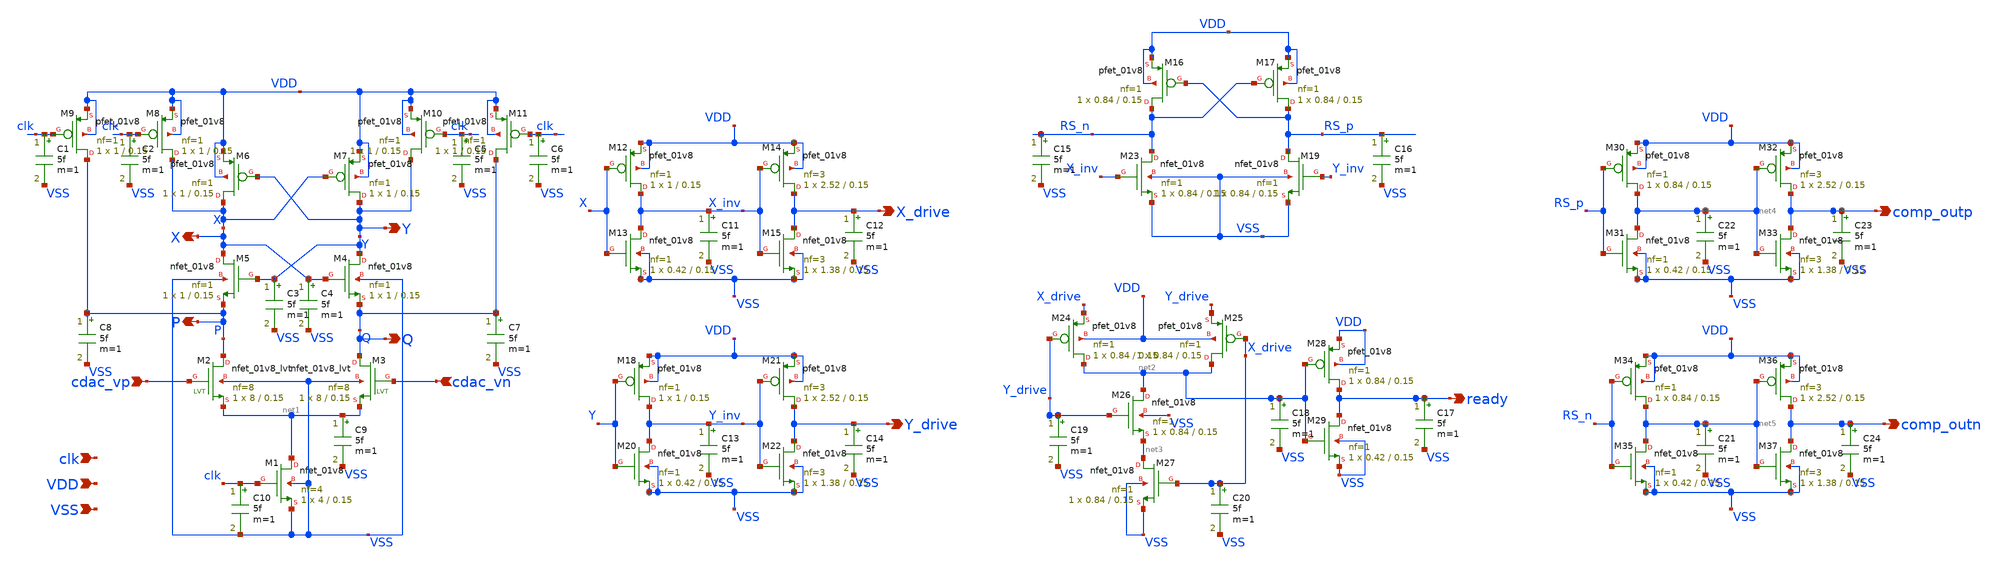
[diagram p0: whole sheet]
** sch_path: hgu/xschem/hgu_comp_withc.sch
**.subckt hgu_comp_withc cdac_vn cdac_vp VSS VDD clk X Y P Q ready X_drive Y_drive comp_outp
*+ comp_outn
*.ipin cdac_vn
*.ipin cdac_vp
*.ipin VSS
*.ipin VDD
*.ipin clk
*.opin X
*.opin Y
*.opin P
*.opin Q
*.opin ready
*.opin X_drive
*.opin Y_drive
*.opin comp_outp
*.opin comp_outn
XM1 net1 clk VSS VSS sky130_fd_pr__nfet_01v8 L=0.15 W=4 nf=4 ad='int((nf+1)/2) * W/nf * 0.29' as='int((nf+2)/2) * W/nf * 0.29'
+ pd='2*int((nf+1)/2) * (W/nf + 0.29)' ps='2*int((nf+2)/2) * (W/nf + 0.29)' nrd='0.29 / W' nrs='0.29 / W'
+ sa=0 sb=0 sd=0 mult=1 m=1
XM4 Y X Q VSS sky130_fd_pr__nfet_01v8 L=0.15 W=1 nf=1 ad='int((nf+1)/2) * W/nf * 0.29' as='int((nf+2)/2) * W/nf * 0.29'
+ pd='2*int((nf+1)/2) * (W/nf + 0.29)' ps='2*int((nf+2)/2) * (W/nf + 0.29)' nrd='0.29 / W' nrs='0.29 / W'
+ sa=0 sb=0 sd=0 mult=1 m=1
XM5 X Y P VSS sky130_fd_pr__nfet_01v8 L=0.15 W=1 nf=1 ad='int((nf+1)/2) * W/nf * 0.29' as='int((nf+2)/2) * W/nf * 0.29'
+ pd='2*int((nf+1)/2) * (W/nf + 0.29)' ps='2*int((nf+2)/2) * (W/nf + 0.29)' nrd='0.29 / W' nrs='0.29 / W'
+ sa=0 sb=0 sd=0 mult=1 m=1
XM6 X Y VDD VDD sky130_fd_pr__pfet_01v8 L=0.15 W=1 nf=1 ad='int((nf+1)/2) * W/nf * 0.29' as='int((nf+2)/2) * W/nf * 0.29'
+ pd='2*int((nf+1)/2) * (W/nf + 0.29)' ps='2*int((nf+2)/2) * (W/nf + 0.29)' nrd='0.29 / W' nrs='0.29 / W'
+ sa=0 sb=0 sd=0 mult=1 m=1
XM7 Y X VDD VDD sky130_fd_pr__pfet_01v8 L=0.15 W=1 nf=1 ad='int((nf+1)/2) * W/nf * 0.29' as='int((nf+2)/2) * W/nf * 0.29'
+ pd='2*int((nf+1)/2) * (W/nf + 0.29)' ps='2*int((nf+2)/2) * (W/nf + 0.29)' nrd='0.29 / W' nrs='0.29 / W'
+ sa=0 sb=0 sd=0 mult=1 m=1
XM8 X clk VDD VDD sky130_fd_pr__pfet_01v8 L=0.15 W=1 nf=1 ad='int((nf+1)/2) * W/nf * 0.29' as='int((nf+2)/2) * W/nf * 0.29'
+ pd='2*int((nf+1)/2) * (W/nf + 0.29)' ps='2*int((nf+2)/2) * (W/nf + 0.29)' nrd='0.29 / W' nrs='0.29 / W'
+ sa=0 sb=0 sd=0 mult=1 m=1
XM9 P clk VDD VDD sky130_fd_pr__pfet_01v8 L=0.15 W=1 nf=1 ad='int((nf+1)/2) * W/nf * 0.29' as='int((nf+2)/2) * W/nf * 0.29'
+ pd='2*int((nf+1)/2) * (W/nf + 0.29)' ps='2*int((nf+2)/2) * (W/nf + 0.29)' nrd='0.29 / W' nrs='0.29 / W'
+ sa=0 sb=0 sd=0 mult=1 m=1
XM10 Y clk VDD VDD sky130_fd_pr__pfet_01v8 L=0.15 W=1 nf=1 ad='int((nf+1)/2) * W/nf * 0.29' as='int((nf+2)/2) * W/nf * 0.29'
+ pd='2*int((nf+1)/2) * (W/nf + 0.29)' ps='2*int((nf+2)/2) * (W/nf + 0.29)' nrd='0.29 / W' nrs='0.29 / W'
+ sa=0 sb=0 sd=0 mult=1 m=1
XM11 Q clk VDD VDD sky130_fd_pr__pfet_01v8 L=0.15 W=1 nf=1 ad='int((nf+1)/2) * W/nf * 0.29' as='int((nf+2)/2) * W/nf * 0.29'
+ pd='2*int((nf+1)/2) * (W/nf + 0.29)' ps='2*int((nf+2)/2) * (W/nf + 0.29)' nrd='0.29 / W' nrs='0.29 / W'
+ sa=0 sb=0 sd=0 mult=1 m=1
XM16 RS_n RS_p VDD VDD sky130_fd_pr__pfet_01v8 L=0.15 W=0.84 nf=1 ad='int((nf+1)/2) * W/nf * 0.29' as='int((nf+2)/2) * W/nf * 0.29'
+ pd='2*int((nf+1)/2) * (W/nf + 0.29)' ps='2*int((nf+2)/2) * (W/nf + 0.29)' nrd='0.29 / W' nrs='0.29 / W'
+ sa=0 sb=0 sd=0 mult=1 m=1
XM17 RS_p RS_n VDD VDD sky130_fd_pr__pfet_01v8 L=0.15 W=0.84 nf=1 ad='int((nf+1)/2) * W/nf * 0.29' as='int((nf+2)/2) * W/nf * 0.29'
+ pd='2*int((nf+1)/2) * (W/nf + 0.29)' ps='2*int((nf+2)/2) * (W/nf + 0.29)' nrd='0.29 / W' nrs='0.29 / W'
+ sa=0 sb=0 sd=0 mult=1 m=1
XM19 RS_p Y_inv VSS VSS sky130_fd_pr__nfet_01v8 L=0.15 W=0.84 nf=1 ad='int((nf+1)/2) * W/nf * 0.29' as='int((nf+2)/2) * W/nf * 0.29'
+ pd='2*int((nf+1)/2) * (W/nf + 0.29)' ps='2*int((nf+2)/2) * (W/nf + 0.29)' nrd='0.29 / W' nrs='0.29 / W'
+ sa=0 sb=0 sd=0 mult=1 m=1
XM23 RS_n X_inv VSS VSS sky130_fd_pr__nfet_01v8 L=0.15 W=0.84 nf=1 ad='int((nf+1)/2) * W/nf * 0.29' as='int((nf+2)/2) * W/nf * 0.29'
+ pd='2*int((nf+1)/2) * (W/nf + 0.29)' ps='2*int((nf+2)/2) * (W/nf + 0.29)' nrd='0.29 / W' nrs='0.29 / W'
+ sa=0 sb=0 sd=0 mult=1 m=1
XM2 P cdac_vp net1 VSS sky130_fd_pr__nfet_01v8_lvt L=0.15 W=8 nf=8 ad='int((nf+1)/2) * W / nf * 0.29'
+ as='int((nf+2)/2) * W / nf * 0.29' pd='2*int((nf+1)/2) * (W / nf + 0.29)' ps='2*int((nf+2)/2) * (W / nf + 0.29)'
+ nrd='0.29 / W ' nrs='0.29 / W ' sa=0 sb=0 sd=0 mult=1 m=1
XM3 Q cdac_vn net1 VSS sky130_fd_pr__nfet_01v8_lvt L=0.15 W=8 nf=8 ad='int((nf+1)/2) * W / nf * 0.29'
+ as='int((nf+2)/2) * W / nf * 0.29' pd='2*int((nf+1)/2) * (W / nf + 0.29)' ps='2*int((nf+2)/2) * (W / nf + 0.29)'
+ nrd='0.29 / W ' nrs='0.29 / W ' sa=0 sb=0 sd=0 mult=1 m=1
XM12 X_inv X VDD VDD sky130_fd_pr__pfet_01v8 L=0.15 W=1 nf=1 ad='int((nf+1)/2) * W/nf * 0.29' as='int((nf+2)/2) * W/nf * 0.29'
+ pd='2*int((nf+1)/2) * (W/nf + 0.29)' ps='2*int((nf+2)/2) * (W/nf + 0.29)' nrd='0.29 / W' nrs='0.29 / W'
+ sa=0 sb=0 sd=0 mult=1 m=1
XM13 X_inv X VSS VSS sky130_fd_pr__nfet_01v8 L=0.15 W=0.42 nf=1 ad='int((nf+1)/2) * W/nf * 0.29' as='int((nf+2)/2) * W/nf * 0.29'
+ pd='2*int((nf+1)/2) * (W/nf + 0.29)' ps='2*int((nf+2)/2) * (W/nf + 0.29)' nrd='0.29 / W' nrs='0.29 / W'
+ sa=0 sb=0 sd=0 mult=1 m=1
XM14 X_drive X_inv VDD VDD sky130_fd_pr__pfet_01v8 L=0.15 W=2.52 nf=3 ad='int((nf+1)/2) * W/nf * 0.29'
+ as='int((nf+2)/2) * W/nf * 0.29' pd='2*int((nf+1)/2) * (W/nf + 0.29)' ps='2*int((nf+2)/2) * (W/nf + 0.29)'
+ nrd='0.29 / W' nrs='0.29 / W' sa=0 sb=0 sd=0 mult=1 m=1
XM15 X_drive X_inv VSS VSS sky130_fd_pr__nfet_01v8 L=0.15 W=1.38 nf=3 ad='int((nf+1)/2) * W/nf * 0.29'
+ as='int((nf+2)/2) * W/nf * 0.29' pd='2*int((nf+1)/2) * (W/nf + 0.29)' ps='2*int((nf+2)/2) * (W/nf + 0.29)'
+ nrd='0.29 / W' nrs='0.29 / W' sa=0 sb=0 sd=0 mult=1 m=1
XM18 Y_inv Y VDD VDD sky130_fd_pr__pfet_01v8 L=0.15 W=1 nf=1 ad='int((nf+1)/2) * W/nf * 0.29' as='int((nf+2)/2) * W/nf * 0.29'
+ pd='2*int((nf+1)/2) * (W/nf + 0.29)' ps='2*int((nf+2)/2) * (W/nf + 0.29)' nrd='0.29 / W' nrs='0.29 / W'
+ sa=0 sb=0 sd=0 mult=1 m=1
XM20 Y_inv Y VSS VSS sky130_fd_pr__nfet_01v8 L=0.15 W=0.42 nf=1 ad='int((nf+1)/2) * W/nf * 0.29' as='int((nf+2)/2) * W/nf * 0.29'
+ pd='2*int((nf+1)/2) * (W/nf + 0.29)' ps='2*int((nf+2)/2) * (W/nf + 0.29)' nrd='0.29 / W' nrs='0.29 / W'
+ sa=0 sb=0 sd=0 mult=1 m=1
XM21 Y_drive Y_inv VDD VDD sky130_fd_pr__pfet_01v8 L=0.15 W=2.52 nf=3 ad='int((nf+1)/2) * W/nf * 0.29'
+ as='int((nf+2)/2) * W/nf * 0.29' pd='2*int((nf+1)/2) * (W/nf + 0.29)' ps='2*int((nf+2)/2) * (W/nf + 0.29)'
+ nrd='0.29 / W' nrs='0.29 / W' sa=0 sb=0 sd=0 mult=1 m=1
XM22 Y_drive Y_inv VSS VSS sky130_fd_pr__nfet_01v8 L=0.15 W=1.38 nf=3 ad='int((nf+1)/2) * W/nf * 0.29'
+ as='int((nf+2)/2) * W/nf * 0.29' pd='2*int((nf+1)/2) * (W/nf + 0.29)' ps='2*int((nf+2)/2) * (W/nf + 0.29)'
+ nrd='0.29 / W' nrs='0.29 / W' sa=0 sb=0 sd=0 mult=1 m=1
XM24 net2 Y_drive X_drive VDD sky130_fd_pr__pfet_01v8 L=0.15 W=0.84 nf=1 ad='int((nf+1)/2) * W/nf * 0.29'
+ as='int((nf+2)/2) * W/nf * 0.29' pd='2*int((nf+1)/2) * (W/nf + 0.29)' ps='2*int((nf+2)/2) * (W/nf + 0.29)'
+ nrd='0.29 / W' nrs='0.29 / W' sa=0 sb=0 sd=0 mult=1 m=1
XM25 net2 X_drive Y_drive VDD sky130_fd_pr__pfet_01v8 L=0.15 W=0.84 nf=1 ad='int((nf+1)/2) * W/nf * 0.29'
+ as='int((nf+2)/2) * W/nf * 0.29' pd='2*int((nf+1)/2) * (W/nf + 0.29)' ps='2*int((nf+2)/2) * (W/nf + 0.29)'
+ nrd='0.29 / W' nrs='0.29 / W' sa=0 sb=0 sd=0 mult=1 m=1
XM26 net2 Y_drive net3 VSS sky130_fd_pr__nfet_01v8 L=0.15 W=0.84 nf=1 ad='int((nf+1)/2) * W/nf * 0.29'
+ as='int((nf+2)/2) * W/nf * 0.29' pd='2*int((nf+1)/2) * (W/nf + 0.29)' ps='2*int((nf+2)/2) * (W/nf + 0.29)'
+ nrd='0.29 / W' nrs='0.29 / W' sa=0 sb=0 sd=0 mult=1 m=1
XM27 net3 X_drive VSS VSS sky130_fd_pr__nfet_01v8 L=0.15 W=0.84 nf=1 ad='int((nf+1)/2) * W/nf * 0.29'
+ as='int((nf+2)/2) * W/nf * 0.29' pd='2*int((nf+1)/2) * (W/nf + 0.29)' ps='2*int((nf+2)/2) * (W/nf + 0.29)'
+ nrd='0.29 / W' nrs='0.29 / W' sa=0 sb=0 sd=0 mult=1 m=1
XM28 ready net2 VDD VDD sky130_fd_pr__pfet_01v8 L=0.15 W=0.84 nf=1 ad='int((nf+1)/2) * W/nf * 0.29' as='int((nf+2)/2) * W/nf * 0.29'
+ pd='2*int((nf+1)/2) * (W/nf + 0.29)' ps='2*int((nf+2)/2) * (W/nf + 0.29)' nrd='0.29 / W' nrs='0.29 / W'
+ sa=0 sb=0 sd=0 mult=1 m=1
XM29 ready net2 VSS VSS sky130_fd_pr__nfet_01v8 L=0.15 W=0.42 nf=1 ad='int((nf+1)/2) * W/nf * 0.29' as='int((nf+2)/2) * W/nf * 0.29'
+ pd='2*int((nf+1)/2) * (W/nf + 0.29)' ps='2*int((nf+2)/2) * (W/nf + 0.29)' nrd='0.29 / W' nrs='0.29 / W'
+ sa=0 sb=0 sd=0 mult=1 m=1
XM30 net4 RS_p VDD VDD sky130_fd_pr__pfet_01v8 L=0.15 W=0.84 nf=1 ad='int((nf+1)/2) * W/nf * 0.29' as='int((nf+2)/2) * W/nf * 0.29'
+ pd='2*int((nf+1)/2) * (W/nf + 0.29)' ps='2*int((nf+2)/2) * (W/nf + 0.29)' nrd='0.29 / W' nrs='0.29 / W'
+ sa=0 sb=0 sd=0 mult=1 m=1
XM31 net4 RS_p VSS VSS sky130_fd_pr__nfet_01v8 L=0.15 W=0.42 nf=1 ad='int((nf+1)/2) * W/nf * 0.29' as='int((nf+2)/2) * W/nf * 0.29'
+ pd='2*int((nf+1)/2) * (W/nf + 0.29)' ps='2*int((nf+2)/2) * (W/nf + 0.29)' nrd='0.29 / W' nrs='0.29 / W'
+ sa=0 sb=0 sd=0 mult=1 m=1
XM32 comp_outp net4 VDD VDD sky130_fd_pr__pfet_01v8 L=0.15 W=2.52 nf=3 ad='int((nf+1)/2) * W/nf * 0.29'
+ as='int((nf+2)/2) * W/nf * 0.29' pd='2*int((nf+1)/2) * (W/nf + 0.29)' ps='2*int((nf+2)/2) * (W/nf + 0.29)'
+ nrd='0.29 / W' nrs='0.29 / W' sa=0 sb=0 sd=0 mult=1 m=1
XM33 comp_outp net4 VSS VSS sky130_fd_pr__nfet_01v8 L=0.15 W=1.38 nf=3 ad='int((nf+1)/2) * W/nf * 0.29'
+ as='int((nf+2)/2) * W/nf * 0.29' pd='2*int((nf+1)/2) * (W/nf + 0.29)' ps='2*int((nf+2)/2) * (W/nf + 0.29)'
+ nrd='0.29 / W' nrs='0.29 / W' sa=0 sb=0 sd=0 mult=1 m=1
XM34 net5 RS_n VDD VDD sky130_fd_pr__pfet_01v8 L=0.15 W=0.84 nf=1 ad='int((nf+1)/2) * W/nf * 0.29' as='int((nf+2)/2) * W/nf * 0.29'
+ pd='2*int((nf+1)/2) * (W/nf + 0.29)' ps='2*int((nf+2)/2) * (W/nf + 0.29)' nrd='0.29 / W' nrs='0.29 / W'
+ sa=0 sb=0 sd=0 mult=1 m=1
XM35 net5 RS_n VSS VSS sky130_fd_pr__nfet_01v8 L=0.15 W=0.42 nf=1 ad='int((nf+1)/2) * W/nf * 0.29' as='int((nf+2)/2) * W/nf * 0.29'
+ pd='2*int((nf+1)/2) * (W/nf + 0.29)' ps='2*int((nf+2)/2) * (W/nf + 0.29)' nrd='0.29 / W' nrs='0.29 / W'
+ sa=0 sb=0 sd=0 mult=1 m=1
XM36 comp_outn net5 VDD VDD sky130_fd_pr__pfet_01v8 L=0.15 W=2.52 nf=3 ad='int((nf+1)/2) * W/nf * 0.29'
+ as='int((nf+2)/2) * W/nf * 0.29' pd='2*int((nf+1)/2) * (W/nf + 0.29)' ps='2*int((nf+2)/2) * (W/nf + 0.29)'
+ nrd='0.29 / W' nrs='0.29 / W' sa=0 sb=0 sd=0 mult=1 m=1
XM37 comp_outn net5 VSS VSS sky130_fd_pr__nfet_01v8 L=0.15 W=1.38 nf=3 ad='int((nf+1)/2) * W/nf * 0.29'
+ as='int((nf+2)/2) * W/nf * 0.29' pd='2*int((nf+1)/2) * (W/nf + 0.29)' ps='2*int((nf+2)/2) * (W/nf + 0.29)'
+ nrd='0.29 / W' nrs='0.29 / W' sa=0 sb=0 sd=0 mult=1 m=1
C1 clk VSS 5f m=1
C2 clk VSS 5f m=1
C3 Y VSS 5f m=1
C4 X VSS 5f m=1
C5 clk VSS 5f m=1
C6 clk VSS 5f m=1
C7 Q VSS 5f m=1
C8 P VSS 5f m=1
C9 net1 VSS 5f m=1
C10 clk VSS 5f m=1
C11 X_inv VSS 5f m=1
C12 X_drive VSS 5f m=1
C13 Y_inv VSS 5f m=1
C14 Y_drive VSS 5f m=1
C15 RS_n VSS 5f m=1
C16 RS_p VSS 5f m=1
C17 ready VSS 5f m=1
C18 net2 VSS 5f m=1
C19 Y_drive VSS 5f m=1
C20 X_drive VSS 5f m=1
C21 net5 VSS 5f m=1
C22 net4 VSS 5f m=1
C23 comp_outp VSS 5f m=1
C24 comp_outn VSS 5f m=1
**.ends
.end
